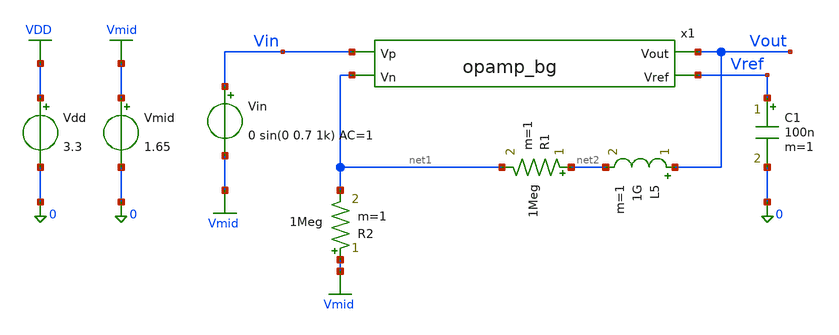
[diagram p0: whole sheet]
** sch_path: xschem/opamp_tb.sch
* Copyright 2021 Stefan Frederik Schippers
* Licensed under the Apache License, Version 2.0 (the "License");
* you may not use this file except in compliance with the License.
* You may obtain a copy of the License at
* https://www.apache.org/licenses/LICENSE-2.0
* Unless required by applicable law or agreed to in writing, software
* distributed under the License is distributed on an "AS IS" BASIS,
* WITHOUT WARRANTIES OR CONDITIONS OF ANY KIND, either express or implied.
* See the License for the specific language governing permissions and
* limitations under the License.
**.subckt opamp_tb
Vdd VDD 0 3.3
C1 Vref 0 100n m=1
Vin Vin Vmid 0 sin(0 0.7 1k) AC=1
R1 net2 net1 1Meg m=1
R2 Vmid net1 1Meg m=1
Vmid Vmid 0 1.65
L5 Vout net2 1G m=1
x1 Vin Vout net1 Vref opamp_bg
**** begin user architecture code

** opencircuitdesign pdks install
.lib $::SKYWATER_MODELS/sky130.lib.spice tt



.option wnflag=1
.option savecurrents
.option rshunt=1e12
.include ../gds/opamp.spice
.save all
.control
set gnuplot_terminal=png/quit
set units = d
op
write opamp_x_tb.raw
print Vref I(v.x1.x2.vmeas_iref) V(x1.x2.Vg1)
if 0
alter L5 1n
tran 1u 2m
plot V(Vin) V(Vout) title 'Vin and Vout vs time'
endif

alter L5 10G
alter L10 10G
ac dec 100 1 100Meg
plot db(V(Vout)) db(V(Vout_mag)) title 'Vout vs Vout_mag Open loop'
*plot cph(V(vout))*180/pi title 'Phase Vout open loop'
gnuplot opamp_ac_mag db(V(Vout))  title 'Open loop gain'  xlabel 'Freq' ylabel 'Gain dB'
gnuplot opamp_ac_phase ph(V(Vout))  title 'Open loop phase'  xlabel 'Freq' ylabel 'Phase (deg)'


if 1
alter L5 1n
alter L10 1n
alter R1 1m
alter R4 1m
ac dec 100 1 100Meg
gnuplot opamp_unity_gain db(V(Vout))  title 'Unity gain bandwidth'  xlabel 'Freq' ylabel 'Gain dB'
gnuplot opamp_unity_gain_phase cph(V(Vout))  title 'Unity gain phase'  xlabel 'Freq' ylabel 'Phase (deg)'

plot db(V(Vout)) title 'Mag Unity gain'
*plot cph(V(vout))*180/pi title 'Phase Vout Unity gain'
endif

.endc


**** end user architecture code
**.ends
.GLOBAL VDD
.GLOBAL Vmid
.end
